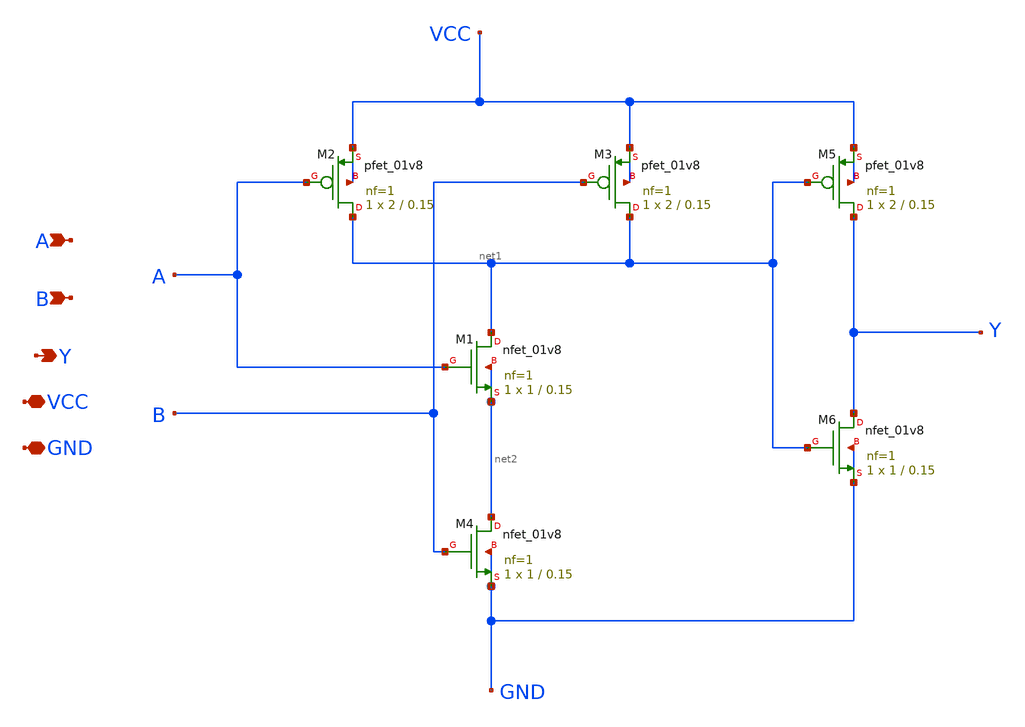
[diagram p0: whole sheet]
** sch_path: xschem/7804_AND_IC.sch
**.subckt 7804_AND_IC A Y B VCC GND
*.ipin A
*.opin Y
*.ipin B
*.iopin VCC
*.iopin GND
XM2 net1 A VCC VCC sky130_fd_pr__pfet_01v8 L=0.15 W=2 nf=1 ad='int((nf+1)/2) * W/nf * 0.29' as='int((nf+2)/2) * W/nf * 0.29'
+ pd='2*int((nf+1)/2) * (W/nf + 0.29)' ps='2*int((nf+2)/2) * (W/nf + 0.29)' nrd='0.29 / W' nrs='0.29 / W'
+ sa=0 sb=0 sd=0 mult=1 m=1
XM3 net1 B VCC VCC sky130_fd_pr__pfet_01v8 L=0.15 W=2 nf=1 ad='int((nf+1)/2) * W/nf * 0.29' as='int((nf+2)/2) * W/nf * 0.29'
+ pd='2*int((nf+1)/2) * (W/nf + 0.29)' ps='2*int((nf+2)/2) * (W/nf + 0.29)' nrd='0.29 / W' nrs='0.29 / W'
+ sa=0 sb=0 sd=0 mult=1 m=1
XM5 Y net1 VCC VCC sky130_fd_pr__pfet_01v8 L=0.15 W=2 nf=1 ad='int((nf+1)/2) * W/nf * 0.29' as='int((nf+2)/2) * W/nf * 0.29'
+ pd='2*int((nf+1)/2) * (W/nf + 0.29)' ps='2*int((nf+2)/2) * (W/nf + 0.29)' nrd='0.29 / W' nrs='0.29 / W'
+ sa=0 sb=0 sd=0 mult=1 m=1
XM1 net1 A net2 net2 sky130_fd_pr__nfet_01v8 L=0.15 W=1 nf=1 ad='int((nf+1)/2) * W/nf * 0.29' as='int((nf+2)/2) * W/nf * 0.29'
+ pd='2*int((nf+1)/2) * (W/nf + 0.29)' ps='2*int((nf+2)/2) * (W/nf + 0.29)' nrd='0.29 / W' nrs='0.29 / W'
+ sa=0 sb=0 sd=0 mult=1 m=1
XM4 net2 B GND GND sky130_fd_pr__nfet_01v8 L=0.15 W=1 nf=1 ad='int((nf+1)/2) * W/nf * 0.29' as='int((nf+2)/2) * W/nf * 0.29'
+ pd='2*int((nf+1)/2) * (W/nf + 0.29)' ps='2*int((nf+2)/2) * (W/nf + 0.29)' nrd='0.29 / W' nrs='0.29 / W'
+ sa=0 sb=0 sd=0 mult=1 m=1
XM6 Y net1 GND GND sky130_fd_pr__nfet_01v8 L=0.15 W=1 nf=1 ad='int((nf+1)/2) * W/nf * 0.29' as='int((nf+2)/2) * W/nf * 0.29'
+ pd='2*int((nf+1)/2) * (W/nf + 0.29)' ps='2*int((nf+2)/2) * (W/nf + 0.29)' nrd='0.29 / W' nrs='0.29 / W'
+ sa=0 sb=0 sd=0 mult=1 m=1
**.ends
.end
